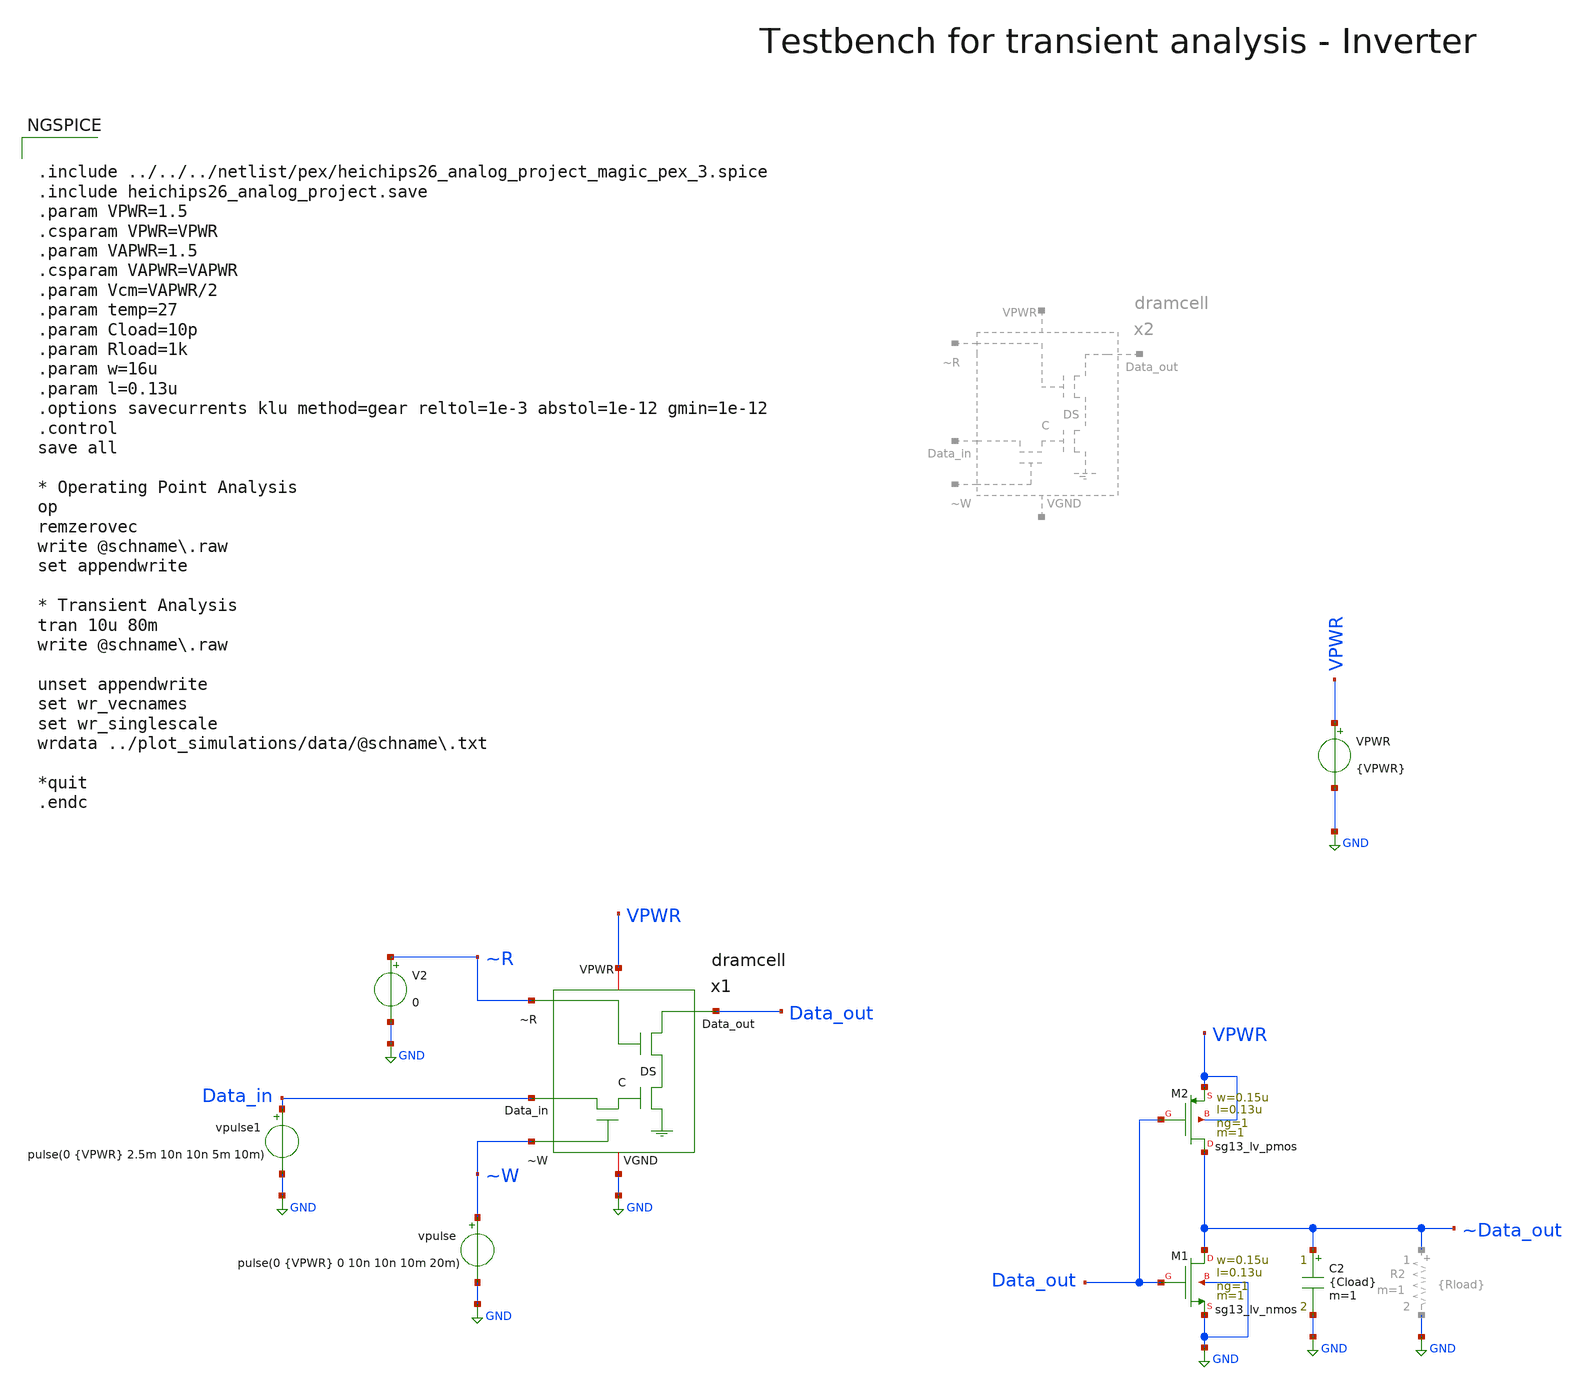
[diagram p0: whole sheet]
** sch_path: macros/heichips26_analog_project/macros/dramcell/testbenches/xschem/inverter_tb_tran.sch
**.subckt inverter_tb_tran
x1 ~W Data_in ~R Data_out GND VPWR dramcell
vpulse ~W GND pulse(0 {VPWR} 0 10n 10n 10m 20m)
V2 ~R GND 0
VPWR VPWR GND {VPWR}
XM1 ~Data_out Data_out GND GND sg13_lv_nmos w=0.15u l=0.13u ng=1 m=1 mm_ok=1
XM2 ~Data_out Data_out VPWR VPWR sg13_lv_pmos w=0.15u l=0.13u ng=1 m=1 mm_ok=1
C2 ~Data_out GND {Cload} m=1
vpulse1 Data_in GND pulse(0 {VPWR} 2.5m 10n 10n 5m 10m)
**** begin user architecture code


.include ../../../netlist/pex/heichips26_analog_project_magic_pex_3.spice
.include heichips26_analog_project.save
.param VPWR=1.5
.csparam VPWR=VPWR
.param VAPWR=1.5
.csparam VAPWR=VAPWR
.param Vcm=VAPWR/2
.param temp=27
.param Cload=10p
.param Rload=1k
.param w=16u
.param l=0.13u
.options savecurrents klu method=gear reltol=1e-3 abstol=1e-12 gmin=1e-12
.control
save all

* Operating Point Analysis
op
remzerovec
write @schname\.raw
set appendwrite

* Transient Analysis
tran 10u 80m
write @schname\.raw

unset appendwrite
set wr_vecnames
set wr_singlescale
wrdata ../plot_simulations/data/@schname\.txt

*quit
.endc



.lib cornerMOSlv.lib mos_tt
.lib cornerMOShv.lib mos_tt
.lib cornerRES.lib res_typ
.lib cornerDIO.lib dio_tt

**** end user architecture code
**.ends
.GLOBAL GND
.end
